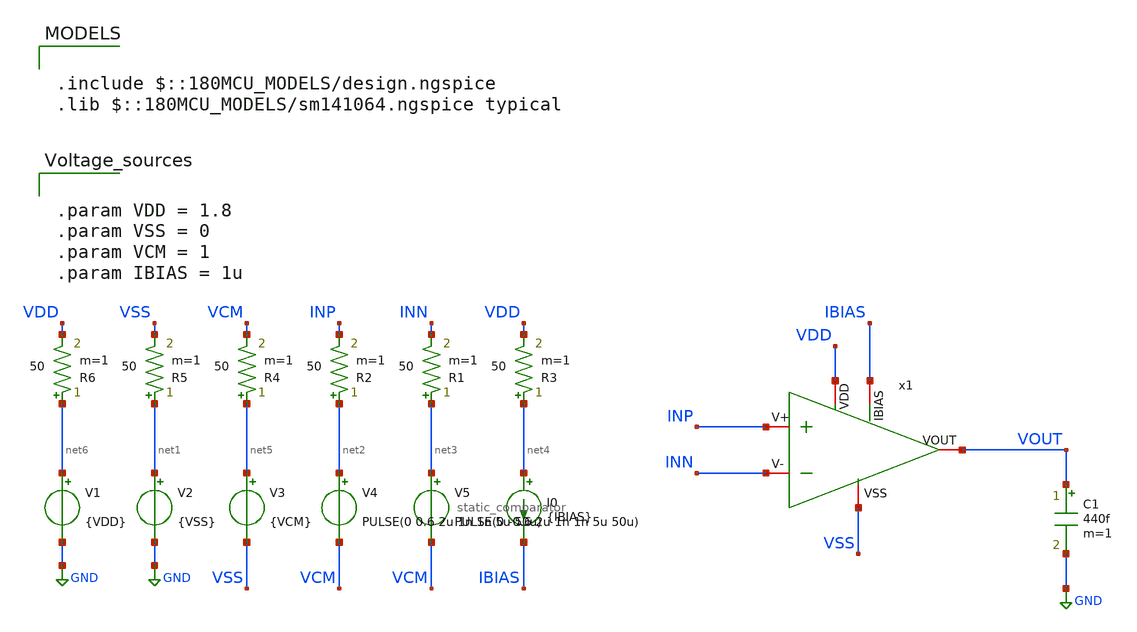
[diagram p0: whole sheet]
** sch_path: designs/static_comparator/xschem/static_comparator_tb_delay.sch
**.subckt static_comparator_tb_delay
V1 net6 GND {VDD}
V4 net2 VCM PULSE(0 0.6 2u 1n 1n 5u 50u)
C1 VOUT GND 440f m=1
V5 net3 VCM PULSE(0 -0.6 2u 1n 1n 5u 50u)
I0 net4 IBIAS {IBIAS}
x1 VDD IBIAS VSS INP INN VOUT static_comparator
V3 net5 VSS {VCM}
V2 net1 GND {VSS}
R3 net4 VDD 50 m=1
R1 net3 INN 50 m=1
R2 net2 INP 50 m=1
R4 net5 VCM 50 m=1
R5 net1 VSS 50 m=1
R6 net6 VDD 50 m=1
**** begin user architecture code

.include $::180MCU_MODELS/design.ngspice
.lib $::180MCU_MODELS/sm141064.ngspice typical




.control
save all

** Simulación transitoria
tran 1u 100u

setplot tran1
let vin  = v(INP) - v(INN)
let vout = v(VOUT)
plot vout vin

**Medir mínimo y máximo de vout

meas tran VOUT_MAX  max vout
meas tran VOUT_MIN  min vout
meas tran VIN_MAX  max vin
meas tran VIN_MIN  min vin

let Vout_medio = (VOUT_MAX + VOUT_MIN)/2
let Vin_medio = (VIN_MAX + VIN_MIN)/2

meas tran T2 WHEN v(vout)= Vout_medio CROSS=1
meas tran T1 WHEN v(vin)= Vin_medio CROSS=1

meas tran T4 WHEN v(vout)= Vout_medio CROSS=2
meas tran T3 WHEN v(vin)= Vin_medio CROSS=2



let tdrise= T2-T1
let tdfall= T4-T3

print tdrise
print tdfall





write comparator_tb_tran.raw
.endc




.param VDD = 1.8
.param VSS = 0
.param VCM = 1
.param IBIAS = 1u


**** end user architecture code
**.ends

* expanding   symbol:  gf180/static_comparator/xschem/static_comparator.sym # of pins=6
** sym_path: gf180/static_comparator/xschem/static_comparator.sym
** sch_path: gf180/static_comparator/xschem/static_comparator.sch
.subckt static_comparator VDD IBIAS VSS V+ V- VOUT
*.iopin IBIAS
*.iopin VSS
*.iopin VDD
*.iopin V+
*.iopin V-
*.iopin VOUT
XM1 IBIAS IBIAS VSS VSS nfet_03v3 L=4u W=1.1u nf=1 ad='int((nf+1)/2) * W/nf * 0.18u' as='int((nf+2)/2) * W/nf * 0.18u'
+ pd='2*int((nf+1)/2) * (W/nf + 0.18u)' ps='2*int((nf+2)/2) * (W/nf + 0.18u)' nrd='0.18u / W' nrs='0.18u / W'
+ sa=0 sb=0 sd=0 m=1
XM3 net1 net1 VDD VDD pfet_03v3 L=2u W=4.5u nf=1 ad='int((nf+1)/2) * W/nf * 0.18u' as='int((nf+2)/2) * W/nf * 0.18u'
+ pd='2*int((nf+1)/2) * (W/nf + 0.18u)' ps='2*int((nf+2)/2) * (W/nf + 0.18u)' nrd='0.18u / W' nrs='0.18u / W'
+ sa=0 sb=0 sd=0 m=1
XM2 net1 IBIAS VSS VSS nfet_03v3 L=4u W=625n nf=1 ad='int((nf+1)/2) * W/nf * 0.18u' as='int((nf+2)/2) * W/nf * 0.18u'
+ pd='2*int((nf+1)/2) * (W/nf + 0.18u)' ps='2*int((nf+2)/2) * (W/nf + 0.18u)' nrd='0.18u / W' nrs='0.18u / W'
+ sa=0 sb=0 sd=0 m=1
XM4 net2 net1 VDD VDD pfet_03v3 L=2u W=25u nf=1 ad='int((nf+1)/2) * W/nf * 0.18u' as='int((nf+2)/2) * W/nf * 0.18u'
+ pd='2*int((nf+1)/2) * (W/nf + 0.18u)' ps='2*int((nf+2)/2) * (W/nf + 0.18u)' nrd='0.18u / W' nrs='0.18u / W'
+ sa=0 sb=0 sd=0 m=1
XM5 Vx+ V+ net2 VDD pfet_03v3 L=360n W=2u nf=1 ad='int((nf+1)/2) * W/nf * 0.18u' as='int((nf+2)/2) * W/nf * 0.18u'
+ pd='2*int((nf+1)/2) * (W/nf + 0.18u)' ps='2*int((nf+2)/2) * (W/nf + 0.18u)' nrd='0.18u / W' nrs='0.18u / W'
+ sa=0 sb=0 sd=0 m=10
XM7 Vx+ Vx+ VSS VSS nfet_03v3 L=2u W=985n nf=1 ad='int((nf+1)/2) * W/nf * 0.18u' as='int((nf+2)/2) * W/nf * 0.18u'
+ pd='2*int((nf+1)/2) * (W/nf + 0.18u)' ps='2*int((nf+2)/2) * (W/nf + 0.18u)' nrd='0.18u / W' nrs='0.18u / W'
+ sa=0 sb=0 sd=0 m=1
XM6 Vx- V- net2 VDD pfet_03v3 L=360n W=2u nf=1 ad='int((nf+1)/2) * W/nf * 0.18u' as='int((nf+2)/2) * W/nf * 0.18u'
+ pd='2*int((nf+1)/2) * (W/nf + 0.18u)' ps='2*int((nf+2)/2) * (W/nf + 0.18u)' nrd='0.18u / W' nrs='0.18u / W'
+ sa=0 sb=0 sd=0 m=10
XM8 Vx- Vx- VSS VSS nfet_03v3 L=2u W=985n nf=1 ad='int((nf+1)/2) * W/nf * 0.18u' as='int((nf+2)/2) * W/nf * 0.18u'
+ pd='2*int((nf+1)/2) * (W/nf + 0.18u)' ps='2*int((nf+2)/2) * (W/nf + 0.18u)' nrd='0.18u / W' nrs='0.18u / W'
+ sa=0 sb=0 sd=0 m=1
XM9 net3 net3 VDD VDD pfet_03v3 L=4u W=950n nf=1 ad='int((nf+1)/2) * W/nf * 0.18u' as='int((nf+2)/2) * W/nf * 0.18u'
+ pd='2*int((nf+1)/2) * (W/nf + 0.18u)' ps='2*int((nf+2)/2) * (W/nf + 0.18u)' nrd='0.18u / W' nrs='0.18u / W'
+ sa=0 sb=0 sd=0 m=1
XM10 VOUT net3 VDD VDD pfet_03v3 L=4u W=950n nf=1 ad='int((nf+1)/2) * W/nf * 0.18u' as='int((nf+2)/2) * W/nf * 0.18u'
+ pd='2*int((nf+1)/2) * (W/nf + 0.18u)' ps='2*int((nf+2)/2) * (W/nf + 0.18u)' nrd='0.18u / W' nrs='0.18u / W'
+ sa=0 sb=0 sd=0 m=1
XM11 net3 Vx- VSS VSS nfet_03v3 L=2u W=1.1u nf=1 ad='int((nf+1)/2) * W/nf * 0.18u' as='int((nf+2)/2) * W/nf * 0.18u'
+ pd='2*int((nf+1)/2) * (W/nf + 0.18u)' ps='2*int((nf+2)/2) * (W/nf + 0.18u)' nrd='0.18u / W' nrs='0.18u / W'
+ sa=0 sb=0 sd=0 m=1
XM12 VOUT Vx+ VSS VSS nfet_03v3 L=2u W=1.1u nf=1 ad='int((nf+1)/2) * W/nf * 0.18u' as='int((nf+2)/2) * W/nf * 0.18u'
+ pd='2*int((nf+1)/2) * (W/nf + 0.18u)' ps='2*int((nf+2)/2) * (W/nf + 0.18u)' nrd='0.18u / W' nrs='0.18u / W'
+ sa=0 sb=0 sd=0 m=1
.ends

.GLOBAL GND
.end
